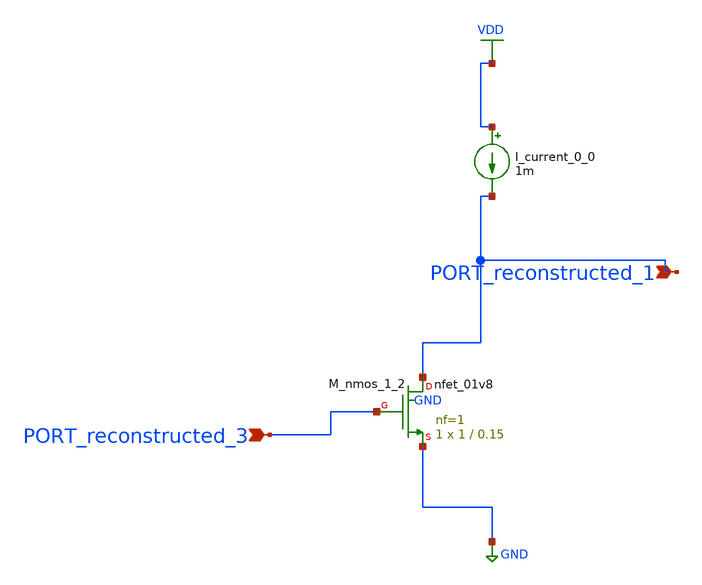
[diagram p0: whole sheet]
** sch_path: schematics/AMSNet/535.sch
**.subckt 535 PORT_reconstructed_3 PORT_reconstructed_1
*.ipin PORT_reconstructed_3
*.ipin PORT_reconstructed_1
I_current_0_0 VDD PORT_reconstructed_1 1m
XM_nmos_1_2 PORT_reconstructed_1 PORT_reconstructed_3 GND GND sky130_fd_pr__nfet_01v8 L=0.15 W=1 nf=1
+ ad='int((1 + 1)/2) * 1 / 1 * 0.29' as='int((1 + 2)/2) * 1 / 1 * 0.29' pd='2*int((1 + 1)/2) * (1 / 1 + 0.29)'
+ ps='2*int((1 + 2)/2) * (1 / 1 + 0.29)' nrd='0.29 / 1 ' nrs='0.29 / 1 ' sa=0 sb=0 sd=0 mult=1 m=1
**.ends
.GLOBAL GND
.GLOBAL VDD
.end
